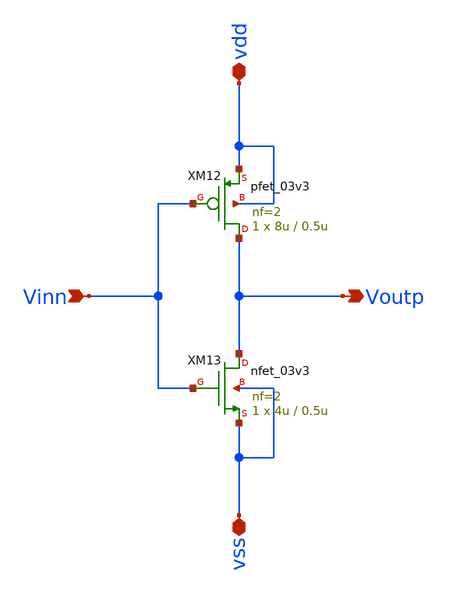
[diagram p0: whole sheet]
** sch_path: xschem/SAR_ADC/xschem/inverter.sch
**.subckt inverter vdd vss Vinn Voutp
*.iopin vdd
*.iopin vss
*.ipin Vinn
*.opin Voutp
XM12 Voutp Vinn vdd vdd pfet_03v3 L=0.5u W=8u nf=2 ad='int((nf+1)/2) * W/nf * 0.18u' as='int((nf+2)/2) * W/nf * 0.18u'
+ pd='2*int((nf+1)/2) * (W/nf + 0.18u)' ps='2*int((nf+2)/2) * (W/nf + 0.18u)' nrd='0.18u / W' nrs='0.18u / W'
+ sa=0 sb=0 sd=0 m=1
XM13 Voutp Vinn vss vss nfet_03v3 L=0.5u W=4u nf=2 ad='int((nf+1)/2) * W/nf * 0.18u' as='int((nf+2)/2) * W/nf * 0.18u'
+ pd='2*int((nf+1)/2) * (W/nf + 0.18u)' ps='2*int((nf+2)/2) * (W/nf + 0.18u)' nrd='0.18u / W' nrs='0.18u / W'
+ sa=0 sb=0 sd=0 m=1
**.ends
.end
